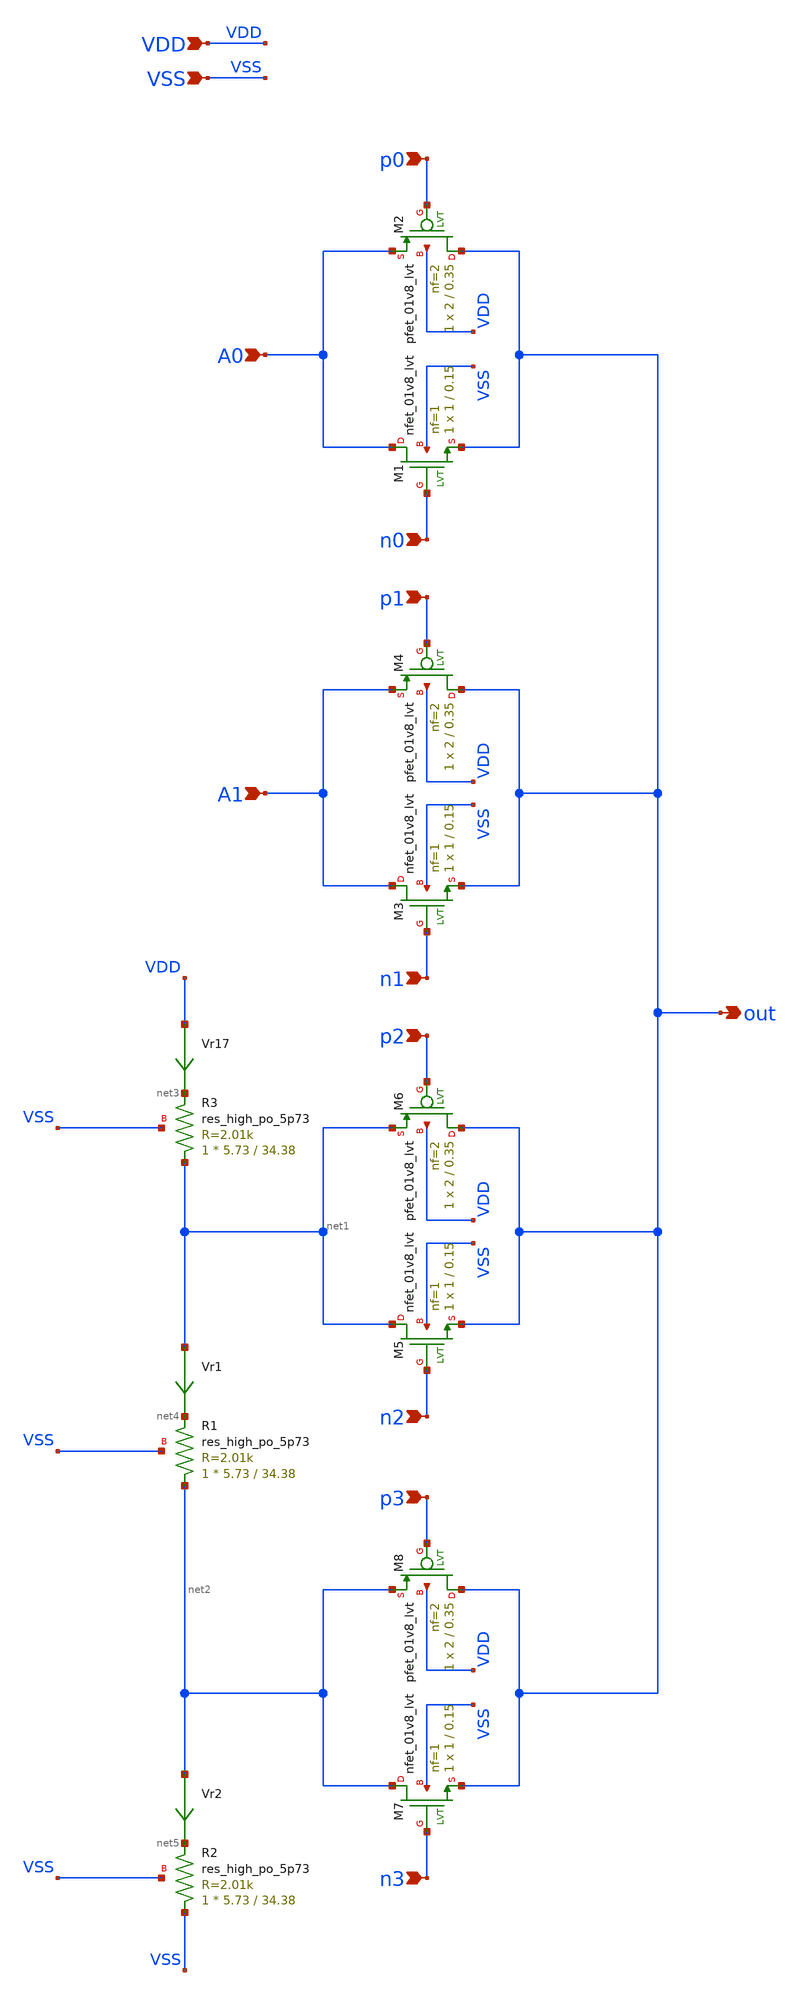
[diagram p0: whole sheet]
** sch_path: xschem/Test_mux_current.sch
**.subckt Test_mux_current A0 out p0 A1 p1 n0 p2 n2 n1 p3 n3 VDD VSS
*.ipin A0
*.opin out
*.ipin p0
*.ipin A1
*.ipin p1
*.ipin n0
*.ipin p2
*.ipin n2
*.ipin n1
*.ipin p3
*.ipin n3
*.ipin VDD
*.ipin VSS
XM1 A0 n0 out VSS sky130_fd_pr__nfet_01v8_lvt L=0.15 W=1 nf=1 ad='int((nf+1)/2) * W/nf * 0.29' as='int((nf+2)/2) * W/nf * 0.29'
+ pd='2*int((nf+1)/2) * (W/nf + 0.29)' ps='2*int((nf+2)/2) * (W/nf + 0.29)' nrd='0.29 / W' nrs='0.29 / W'
+ sa=0 sb=0 sd=0 mult=1 m=1
XM2 out p0 A0 VDD sky130_fd_pr__pfet_01v8_lvt L=0.35 W=2 nf=2 ad='int((nf+1)/2) * W/nf * 0.29' as='int((nf+2)/2) * W/nf * 0.29'
+ pd='2*int((nf+1)/2) * (W/nf + 0.29)' ps='2*int((nf+2)/2) * (W/nf + 0.29)' nrd='0.29 / W' nrs='0.29 / W'
+ sa=0 sb=0 sd=0 mult=1 m=1
XM3 A1 n1 out VSS sky130_fd_pr__nfet_01v8_lvt L=0.15 W=1 nf=1 ad='int((nf+1)/2) * W/nf * 0.29' as='int((nf+2)/2) * W/nf * 0.29'
+ pd='2*int((nf+1)/2) * (W/nf + 0.29)' ps='2*int((nf+2)/2) * (W/nf + 0.29)' nrd='0.29 / W' nrs='0.29 / W'
+ sa=0 sb=0 sd=0 mult=1 m=1
XM4 out p1 A1 VDD sky130_fd_pr__pfet_01v8_lvt L=0.35 W=2 nf=2 ad='int((nf+1)/2) * W/nf * 0.29' as='int((nf+2)/2) * W/nf * 0.29'
+ pd='2*int((nf+1)/2) * (W/nf + 0.29)' ps='2*int((nf+2)/2) * (W/nf + 0.29)' nrd='0.29 / W' nrs='0.29 / W'
+ sa=0 sb=0 sd=0 mult=1 m=1
XM5 net1 n2 out VSS sky130_fd_pr__nfet_01v8_lvt L=0.15 W=1 nf=1 ad='int((nf+1)/2) * W/nf * 0.29' as='int((nf+2)/2) * W/nf * 0.29'
+ pd='2*int((nf+1)/2) * (W/nf + 0.29)' ps='2*int((nf+2)/2) * (W/nf + 0.29)' nrd='0.29 / W' nrs='0.29 / W'
+ sa=0 sb=0 sd=0 mult=1 m=1
XM6 out p2 net1 VDD sky130_fd_pr__pfet_01v8_lvt L=0.35 W=2 nf=2 ad='int((nf+1)/2) * W/nf * 0.29' as='int((nf+2)/2) * W/nf * 0.29'
+ pd='2*int((nf+1)/2) * (W/nf + 0.29)' ps='2*int((nf+2)/2) * (W/nf + 0.29)' nrd='0.29 / W' nrs='0.29 / W'
+ sa=0 sb=0 sd=0 mult=1 m=1
XM7 net2 n3 out VSS sky130_fd_pr__nfet_01v8_lvt L=0.15 W=1 nf=1 ad='int((nf+1)/2) * W/nf * 0.29' as='int((nf+2)/2) * W/nf * 0.29'
+ pd='2*int((nf+1)/2) * (W/nf + 0.29)' ps='2*int((nf+2)/2) * (W/nf + 0.29)' nrd='0.29 / W' nrs='0.29 / W'
+ sa=0 sb=0 sd=0 mult=1 m=1
XM8 out p3 net2 VDD sky130_fd_pr__pfet_01v8_lvt L=0.35 W=2 nf=2 ad='int((nf+1)/2) * W/nf * 0.29' as='int((nf+2)/2) * W/nf * 0.29'
+ pd='2*int((nf+1)/2) * (W/nf + 0.29)' ps='2*int((nf+2)/2) * (W/nf + 0.29)' nrd='0.29 / W' nrs='0.29 / W'
+ sa=0 sb=0 sd=0 mult=1 m=1
XR3 net1 net3 VSS sky130_fd_pr__res_high_po_5p73 L=34.38 mult=1 m=1
XR1 net2 net4 VSS sky130_fd_pr__res_high_po_5p73 L=34.38 mult=1 m=1
XR2 VSS net5 VSS sky130_fd_pr__res_high_po_5p73 L=34.38 mult=1 m=1
Vr17 VDD net3 0
.save i(vr17)
Vr1 net1 net4 0
.save i(vr1)
Vr2 net2 net5 0
.save i(vr2)
**.ends
.end
